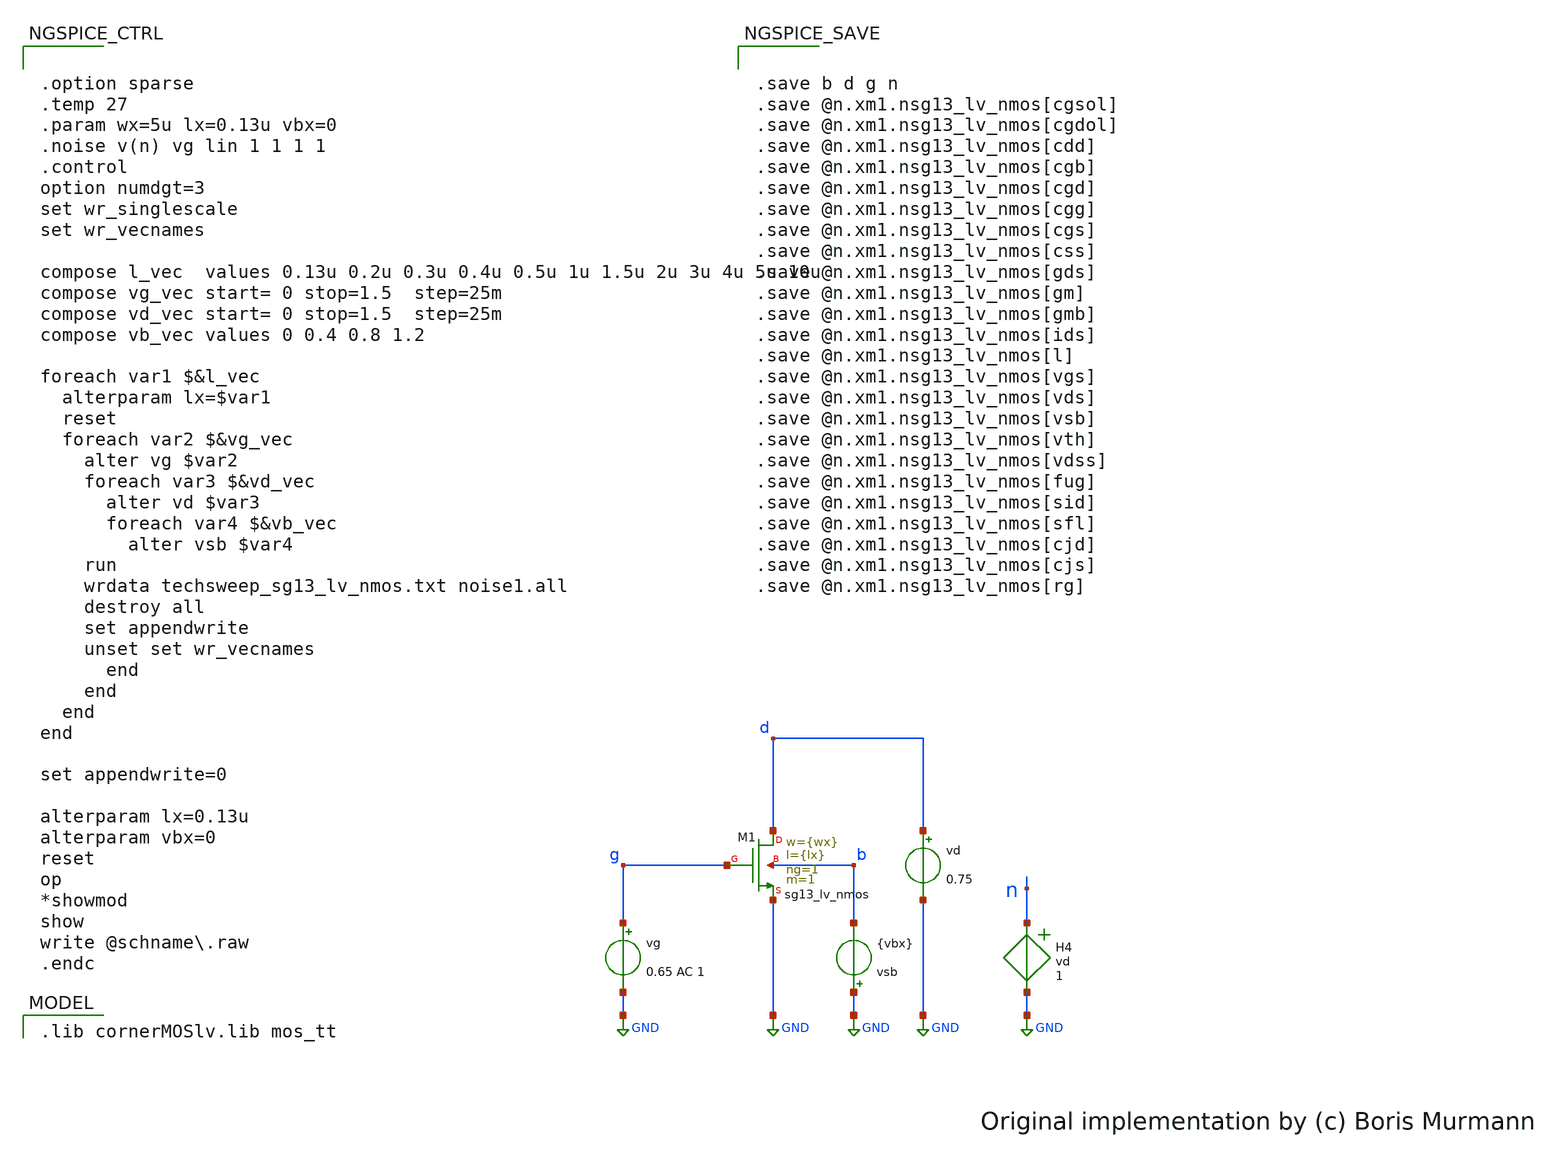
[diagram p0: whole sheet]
** sch_path: xschem/techsweep_sg13cmos5l_lv_nmos.sch
* (c) 2024-2025 Harald Pretl, Apache-2.0 license
**.subckt techsweep_sg13cmos5l_lv_nmos
vg g GND 0.65 AC 1
vd d GND 0.75
XM1 d g GND b sg13_lv_nmos w={wx} l={lx} ng=1 m=1 mm_ok=1
vsb GND b {vbx}
H4 n GND vd 1
**** begin user architecture code
 .lib cornerMOSlv.lib mos_tt



.option sparse
.temp 27
.param wx=5u lx=0.13u vbx=0
.noise v(n) vg lin 1 1 1 1
.control
option numdgt=3
set wr_singlescale
set wr_vecnames

compose l_vec  values 0.13u 0.2u 0.3u 0.4u 0.5u 1u 1.5u 2u 3u 4u 5u 10u
compose vg_vec start= 0 stop=1.5  step=25m
compose vd_vec start= 0 stop=1.5  step=25m
compose vb_vec values 0 0.4 0.8 1.2

foreach var1 $&l_vec
  alterparam lx=$var1
  reset
  foreach var2 $&vg_vec
    alter vg $var2
    foreach var3 $&vd_vec
      alter vd $var3
      foreach var4 $&vb_vec
        alter vsb $var4
	run
	wrdata techsweep_sg13_lv_nmos.txt noise1.all
	destroy all
	set appendwrite
	unset set wr_vecnames
      end
    end
  end
end

set appendwrite=0

alterparam lx=0.13u
alterparam vbx=0
reset
op
*showmod
show
write @schname\.raw
.endc




.save b d g n
.save @n.xm1.nsg13_lv_nmos[cgsol]
.save @n.xm1.nsg13_lv_nmos[cgdol]
.save @n.xm1.nsg13_lv_nmos[cdd]
.save @n.xm1.nsg13_lv_nmos[cgb]
.save @n.xm1.nsg13_lv_nmos[cgd]
.save @n.xm1.nsg13_lv_nmos[cgg]
.save @n.xm1.nsg13_lv_nmos[cgs]
.save @n.xm1.nsg13_lv_nmos[css]
.save @n.xm1.nsg13_lv_nmos[gds]
.save @n.xm1.nsg13_lv_nmos[gm]
.save @n.xm1.nsg13_lv_nmos[gmb]
.save @n.xm1.nsg13_lv_nmos[ids]
.save @n.xm1.nsg13_lv_nmos[l]
.save @n.xm1.nsg13_lv_nmos[vgs]
.save @n.xm1.nsg13_lv_nmos[vds]
.save @n.xm1.nsg13_lv_nmos[vsb]
.save @n.xm1.nsg13_lv_nmos[vth]
.save @n.xm1.nsg13_lv_nmos[vdss]
.save @n.xm1.nsg13_lv_nmos[fug]
.save @n.xm1.nsg13_lv_nmos[sid]
.save @n.xm1.nsg13_lv_nmos[sfl]
.save @n.xm1.nsg13_lv_nmos[cjd]
.save @n.xm1.nsg13_lv_nmos[cjs]
.save @n.xm1.nsg13_lv_nmos[rg]


**** end user architecture code
**.ends
.GLOBAL GND
.end
